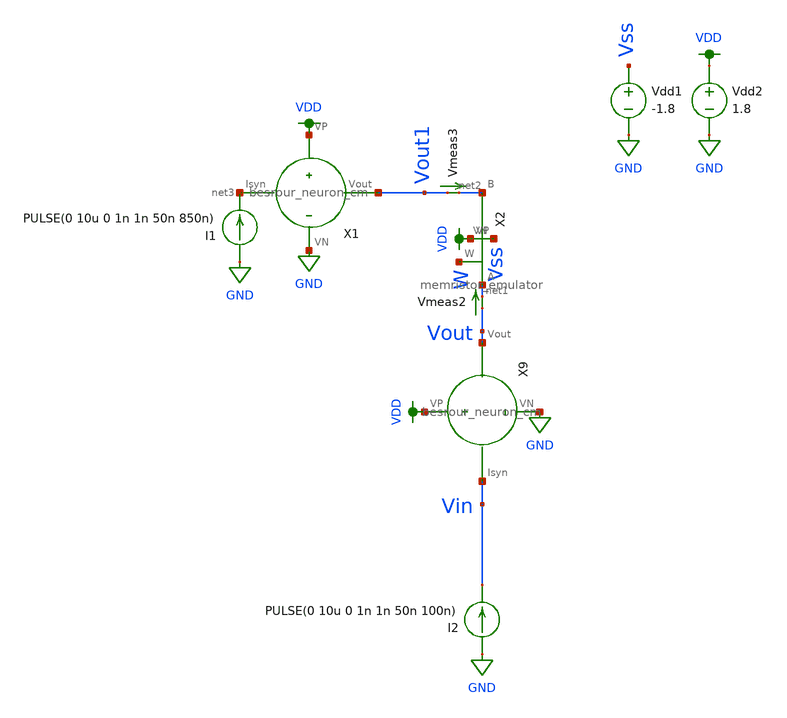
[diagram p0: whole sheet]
** sch_path: schematic/crossbar_1.sch
**.subckt crossbar_1
Vdd1 Vss GND -1.8
X9 Vin Vout VDD GND besrour_neuron_cm
Vmeas2 Vout net1 0
.save i(vmeas2)
I2 GND Vin PULSE(0 10u 0 1n 1n 50n 100n)
X1 net3 Vout1 VDD GND besrour_neuron_cm
I1 GND net3 PULSE(0 10u 0 1n 1n 50n 850n)
Vdd2 VDD GND 1.8
X2 VDD Vss net2 net1 W memristor_emulator
Vmeas3 Vout1 net2 0
.save i(vmeas3)
**** begin user architecture code

.option wnflag=1
.param MC_SWITCH=0.0
.lib ~/skywater/skywater-pdk/libraries/sky130_fd_pr_ngspice/latest/models/sky130.lib.spice tt


.param W=12
.param L=0.5
.tran 1n 100u
.save all

**** end user architecture code
**.ends

* expanding   symbol:  /home/madvlsi/neuromorphic_computing_final/schematic/besrour_neuron_cm.sym #
*+ of pins=4
** sym_path: schematic/besrour_neuron_cm.sym
** sch_path: schematic/besrour_neuron_cm.sch
.subckt besrour_neuron_cm Isyn Vout VP VN
*.iopin VP
*.iopin VN
*.iopin Isyn
*.opin Vout
XM2 VMEMINT net1 VP VDD sky130_fd_pr__pfet_01v8 L={L} W={W} nf=1 ad='int((nf+1)/2) * W/nf * 0.29' as='int((nf+2)/2) * W/nf * 0.29'
+ pd='2*int((nf+1)/2) * (W/nf + 0.29)' ps='2*int((nf+2)/2) * (W/nf + 0.29)' nrd='0.29 / W' nrs='0.29 / W'
+ sa=0 sb=0 sd=0 mult=1 m=1
XM3 VP net3 VMEMINT VDD sky130_fd_pr__pfet_01v8 L={L} W={W} nf=1 ad='int((nf+1)/2) * W/nf * 0.29' as='int((nf+2)/2) * W/nf * 0.29'
+ pd='2*int((nf+1)/2) * (W/nf + 0.29)' ps='2*int((nf+2)/2) * (W/nf + 0.29)' nrd='0.29 / W' nrs='0.29 / W'
+ sa=0 sb=0 sd=0 mult=1 m=1
XM4 net3 VMEMINT VP VDD sky130_fd_pr__pfet_01v8 L={L} W={W} nf=1 ad='int((nf+1)/2) * W/nf * 0.29' as='int((nf+2)/2) * W/nf * 0.29'
+ pd='2*int((nf+1)/2) * (W/nf + 0.29)' ps='2*int((nf+2)/2) * (W/nf + 0.29)' nrd='0.29 / W' nrs='0.29 / W'
+ sa=0 sb=0 sd=0 mult=1 m=1
XM5 net2 net3 VP VDD sky130_fd_pr__pfet_01v8 L={L} W={W} nf=1 ad='int((nf+1)/2) * W/nf * 0.29' as='int((nf+2)/2) * W/nf * 0.29'
+ pd='2*int((nf+1)/2) * (W/nf + 0.29)' ps='2*int((nf+2)/2) * (W/nf + 0.29)' nrd='0.29 / W' nrs='0.29 / W'
+ sa=0 sb=0 sd=0 mult=1 m=1
XM6 net3 VMEMINT VN GND sky130_fd_pr__nfet_01v8 L={L} W={W} nf=1 ad='int((nf+1)/2) * W/nf * 0.29' as='int((nf+2)/2) * W/nf * 0.29'
+ pd='2*int((nf+1)/2) * (W/nf + 0.29)' ps='2*int((nf+2)/2) * (W/nf + 0.29)' nrd='0.29 / W' nrs='0.29 / W'
+ sa=0 sb=0 sd=0 mult=1 m=1
XM8 net2 net3 VN GND sky130_fd_pr__nfet_01v8 L={L} W={W} nf=1 ad='int((nf+1)/2) * W/nf * 0.29' as='int((nf+2)/2) * W/nf * 0.29'
+ pd='2*int((nf+1)/2) * (W/nf + 0.29)' ps='2*int((nf+2)/2) * (W/nf + 0.29)' nrd='0.29 / W' nrs='0.29 / W'
+ sa=0 sb=0 sd=0 mult=1 m=1
C1 VMEMINT VN 340f m=1
C2 net2 VN 340f m=1
XM9 net4 net2 VP VDD sky130_fd_pr__pfet_01v8 L={L} W={W} nf=1 ad='int((nf+1)/2) * W/nf * 0.29' as='int((nf+2)/2) * W/nf * 0.29'
+ pd='2*int((nf+1)/2) * (W/nf + 0.29)' ps='2*int((nf+2)/2) * (W/nf + 0.29)' nrd='0.29 / W' nrs='0.29 / W'
+ sa=0 sb=0 sd=0 mult=1 m=1
XM10 net4 net2 VN GND sky130_fd_pr__nfet_01v8 L={L} W={W} nf=1 ad='int((nf+1)/2) * W/nf * 0.29' as='int((nf+2)/2) * W/nf * 0.29'
+ pd='2*int((nf+1)/2) * (W/nf + 0.29)' ps='2*int((nf+2)/2) * (W/nf + 0.29)' nrd='0.29 / W' nrs='0.29 / W'
+ sa=0 sb=0 sd=0 mult=1 m=1
XM11 Vout net4 VP VDD sky130_fd_pr__pfet_01v8 L={L} W={W} nf=1 ad='int((nf+1)/2) * W/nf * 0.29' as='int((nf+2)/2) * W/nf * 0.29'
+ pd='2*int((nf+1)/2) * (W/nf + 0.29)' ps='2*int((nf+2)/2) * (W/nf + 0.29)' nrd='0.29 / W' nrs='0.29 / W'
+ sa=0 sb=0 sd=0 mult=1 m=1
XM12 Vout net4 VN GND sky130_fd_pr__nfet_01v8 L={L} W={W} nf=1 ad='int((nf+1)/2) * W/nf * 0.29' as='int((nf+2)/2) * W/nf * 0.29'
+ pd='2*int((nf+1)/2) * (W/nf + 0.29)' ps='2*int((nf+2)/2) * (W/nf + 0.29)' nrd='0.29 / W' nrs='0.29 / W'
+ sa=0 sb=0 sd=0 mult=1 m=1
XM13 net1 Isyn VN GND sky130_fd_pr__nfet_01v8 L={L} W={W} nf=1 ad='int((nf+1)/2) * W/nf * 0.29' as='int((nf+2)/2) * W/nf * 0.29'
+ pd='2*int((nf+1)/2) * (W/nf + 0.29)' ps='2*int((nf+2)/2) * (W/nf + 0.29)' nrd='0.29 / W' nrs='0.29 / W'
+ sa=0 sb=0 sd=0 mult=1 m=1
XM14 VN Isyn Isyn GND sky130_fd_pr__nfet_01v8 L={L} W={W} nf=1 ad='int((nf+1)/2) * W/nf * 0.29' as='int((nf+2)/2) * W/nf * 0.29'
+ pd='2*int((nf+1)/2) * (W/nf + 0.29)' ps='2*int((nf+2)/2) * (W/nf + 0.29)' nrd='0.29 / W' nrs='0.29 / W'
+ sa=0 sb=0 sd=0 mult=1 m=1
XM1 VP net1 net1 VDD sky130_fd_pr__pfet_01v8 L={L} W={W} nf=1 ad='int((nf+1)/2) * W/nf * 0.29' as='int((nf+2)/2) * W/nf * 0.29'
+ pd='2*int((nf+1)/2) * (W/nf + 0.29)' ps='2*int((nf+2)/2) * (W/nf + 0.29)' nrd='0.29 / W' nrs='0.29 / W'
+ sa=0 sb=0 sd=0 mult=1 m=1
XM7 VN net2 VMEMINT GND sky130_fd_pr__nfet_01v8 L={L} W={W} nf=1 ad='int((nf+1)/2) * W/nf * 0.29' as='int((nf+2)/2) * W/nf * 0.29'
+ pd='2*int((nf+1)/2) * (W/nf + 0.29)' ps='2*int((nf+2)/2) * (W/nf + 0.29)' nrd='0.29 / W' nrs='0.29 / W'
+ sa=0 sb=0 sd=0 mult=1 m=1
.ends


* expanding   symbol:  /home/madvlsi/neuromorphic_computing_final/schematic/memristor_emulator.sym #
*+ of pins=5
** sym_path: schematic/memristor_emulator.sym
** sch_path: schematic/memristor_emulator.sch
.subckt memristor_emulator VP VN B A W
*.iopin VN
*.iopin VP
*.opin W
*.iopin B
*.iopin A
XM1 B W A B sky130_fd_pr__pfet_01v8 L=0.5 W=12 nf=1 ad='int((nf+1)/2) * W/nf * 0.29' as='int((nf+2)/2) * W/nf * 0.29'
+ pd='2*int((nf+1)/2) * (W/nf + 0.29)' ps='2*int((nf+2)/2) * (W/nf + 0.29)' nrd='0.29 / W' nrs='0.29 / W'
+ sa=0 sb=0 sd=0 mult=1 m=1
XM2 VP A W VP sky130_fd_pr__pfet_01v8 L=2 W=3 nf=1 ad='int((nf+1)/2) * W/nf * 0.29' as='int((nf+2)/2) * W/nf * 0.29'
+ pd='2*int((nf+1)/2) * (W/nf + 0.29)' ps='2*int((nf+2)/2) * (W/nf + 0.29)' nrd='0.29 / W' nrs='0.29 / W'
+ sa=0 sb=0 sd=0 mult=1 m=1
XM3 VN W VN VN sky130_fd_pr__nfet_01v8 L=20 W=20 nf=1 ad='int((nf+1)/2) * W/nf * 0.29' as='int((nf+2)/2) * W/nf * 0.29'
+ pd='2*int((nf+1)/2) * (W/nf + 0.29)' ps='2*int((nf+2)/2) * (W/nf + 0.29)' nrd='0.29 / W' nrs='0.29 / W'
+ sa=0 sb=0 sd=0 mult=1 m=1
XM4 VN B W VN sky130_fd_pr__nfet_01v8 L=3 W=2 nf=1 ad='int((nf+1)/2) * W/nf * 0.29' as='int((nf+2)/2) * W/nf * 0.29'
+ pd='2*int((nf+1)/2) * (W/nf + 0.29)' ps='2*int((nf+2)/2) * (W/nf + 0.29)' nrd='0.29 / W' nrs='0.29 / W'
+ sa=0 sb=0 sd=0 mult=1 m=1
.ends

.GLOBAL VDD
.GLOBAL GND
.end
